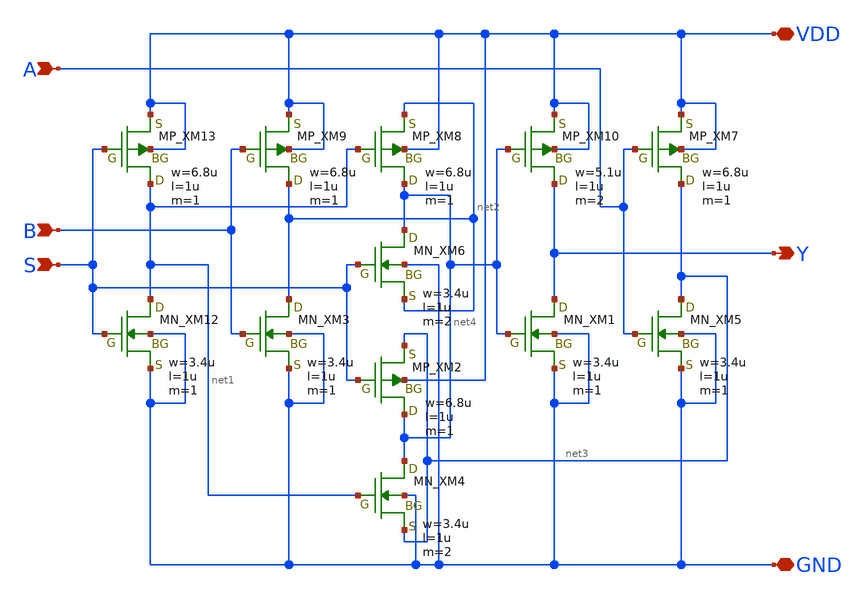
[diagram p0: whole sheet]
** sch_path: openIP62_rev1.0/IP62/Technology/tech/symbols/Xschem/IP62_5_stdcell/MUX2.sch
**.subckt MUX2 B S Y VDD GND A
*.ipin B
*.ipin S
*.opin Y
*.iopin VDD
*.iopin GND
*.ipin A
XM13 net1 S VDD VDD PMOS w=6.8u l=1u as=0 ad=0 ps=0 pd=0 nrd=0 nrs=0 m=1
XM9 net2 B VDD VDD PMOS w=6.8u l=1u as=0 ad=0 ps=0 pd=0 nrd=0 nrs=0 m=1
XM8 net4 net1 net2 VDD PMOS w=6.8u l=1u as=0 ad=0 ps=0 pd=0 nrd=0 nrs=0 m=1
XM10 Y net4 VDD VDD PMOS w=5.1u l=1u as=0 ad=0 ps=0 pd=0 nrd=0 nrs=0 m=2
XM2 net4 S net3 VDD PMOS w=6.8u l=1u as=0 ad=0 ps=0 pd=0 nrd=0 nrs=0 m=1
XM12 net1 S GND GND NMOS w=3.4u l=1u as=0 ad=0 ps=0 pd=0 nrd=0 nrs=0 m=1
XM3 net2 B GND GND NMOS w=3.4u l=1u as=0 ad=0 ps=0 pd=0 nrd=0 nrs=0 m=1
XM1 Y net4 GND GND NMOS w=3.4u l=1u as=0 ad=0 ps=0 pd=0 nrd=0 nrs=0 m=1
XM5 net3 A GND GND NMOS w=3.4u l=1u as=0 ad=0 ps=0 pd=0 nrd=0 nrs=0 m=1
XM6 net4 S net2 GND NMOS w=3.4u l=1u as=0 ad=0 ps=0 pd=0 nrd=0 nrs=0 m=2
XM4 net4 net1 net3 GND NMOS w=3.4u l=1u as=0 ad=0 ps=0 pd=0 nrd=0 nrs=0 m=2
XM7 net3 A VDD VDD PMOS w=6.8u l=1u as=0 ad=0 ps=0 pd=0 nrd=0 nrs=0 m=1
**.ends
.end
